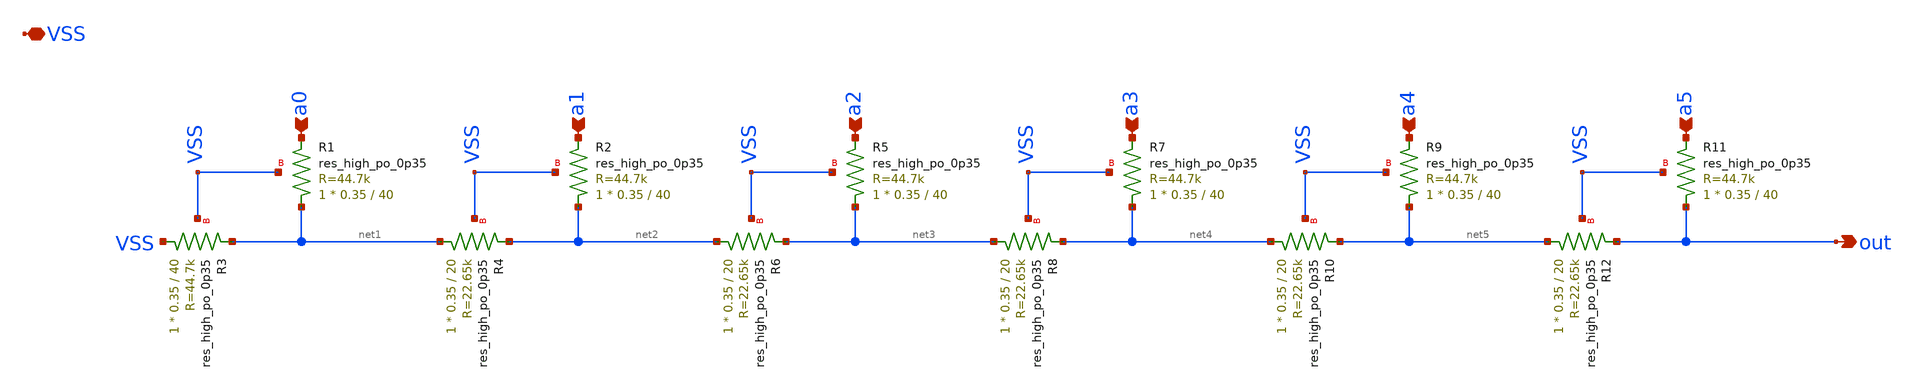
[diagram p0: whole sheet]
** sch_path: xschem/dac_6b.sch
**.subckt dac_6b VSS a0 a1 a2 a3 a4 a5 out
*.iopin VSS
*.ipin a0
*.ipin a1
*.ipin a2
*.ipin a3
*.ipin a4
*.ipin a5
*.opin out
XR1 net1 a0 VSS sky130_fd_pr__res_high_po_0p35 L=40 mult=1 m=1
XR3 VSS net1 VSS sky130_fd_pr__res_high_po_0p35 L=40 mult=1 m=1
XR2 net2 a1 VSS sky130_fd_pr__res_high_po_0p35 L=40 mult=1 m=1
XR4 net1 net2 VSS sky130_fd_pr__res_high_po_0p35 L=20 mult=1 m=1
XR5 net3 a2 VSS sky130_fd_pr__res_high_po_0p35 L=40 mult=1 m=1
XR6 net2 net3 VSS sky130_fd_pr__res_high_po_0p35 L=20 mult=1 m=1
XR7 net4 a3 VSS sky130_fd_pr__res_high_po_0p35 L=40 mult=1 m=1
XR8 net3 net4 VSS sky130_fd_pr__res_high_po_0p35 L=20 mult=1 m=1
XR9 net5 a4 VSS sky130_fd_pr__res_high_po_0p35 L=40 mult=1 m=1
XR10 net4 net5 VSS sky130_fd_pr__res_high_po_0p35 L=20 mult=1 m=1
XR11 out a5 VSS sky130_fd_pr__res_high_po_0p35 L=40 mult=1 m=1
XR12 net5 out VSS sky130_fd_pr__res_high_po_0p35 L=20 mult=1 m=1
**.ends
.end
